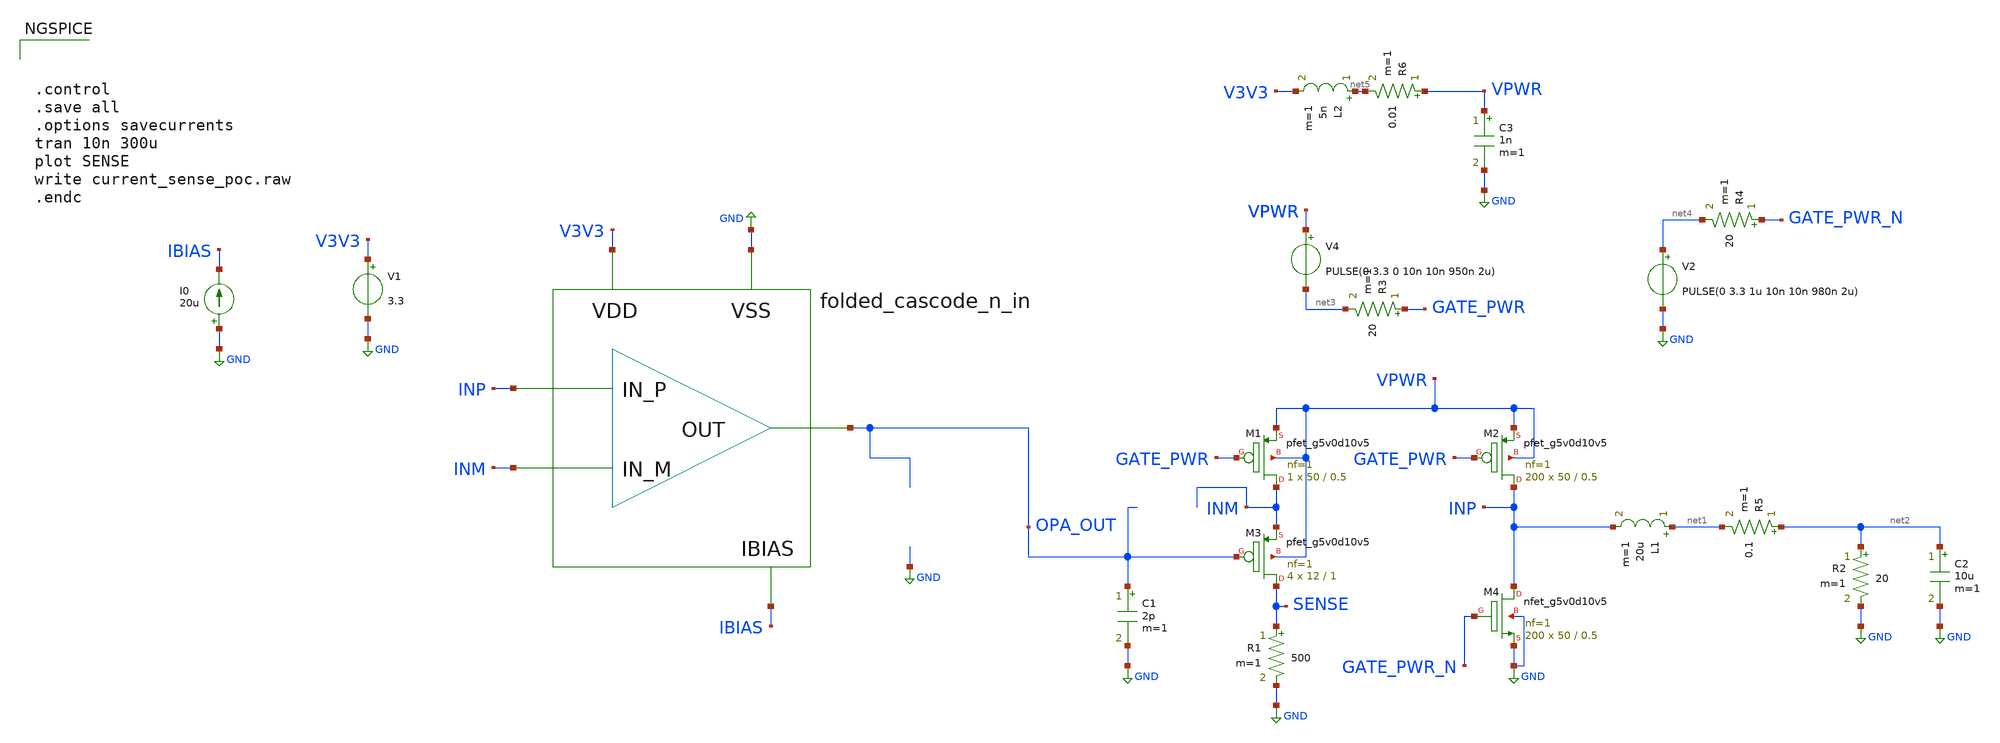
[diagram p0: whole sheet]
** sch_path: design/current-sense/current_sense_poc.sch
**.subckt current_sense_poc
V1 V3V3 GND 3.3
I0 GND IBIAS 20u
x1 INP INM OPA_OUT V3V3 GND IBIAS folded_cascode_n_in
XM1 INM GATE_PWR VPWR VPWR sky130_fd_pr__pfet_g5v0d10v5 L=0.5 W=50 nf=1 ad='int((nf+1)/2) * W/nf * 0.29'
+ as='int((nf+2)/2) * W/nf * 0.29' pd='2*int((nf+1)/2) * (W/nf + 0.29)' ps='2*int((nf+2)/2) * (W/nf + 0.29)'
+ nrd='0.29 / W' nrs='0.29 / W' sa=0 sb=0 sd=0 mult=1 m=1
XM2 INP GATE_PWR VPWR VPWR sky130_fd_pr__pfet_g5v0d10v5 L=0.5 W=50 nf=1 ad='int((nf+1)/2) * W/nf * 0.29'
+ as='int((nf+2)/2) * W/nf * 0.29' pd='2*int((nf+1)/2) * (W/nf + 0.29)' ps='2*int((nf+2)/2) * (W/nf + 0.29)'
+ nrd='0.29 / W' nrs='0.29 / W' sa=0 sb=0 sd=0 mult=200 m=200
V4 VPWR net3 PULSE(0 3.3 0 10n 10n 950n 2u)
XM3 SENSE OPA_OUT INM VPWR sky130_fd_pr__pfet_g5v0d10v5 L=1 W=12 nf=1 ad='int((nf+1)/2) * W/nf * 0.29'
+ as='int((nf+2)/2) * W/nf * 0.29' pd='2*int((nf+1)/2) * (W/nf + 0.29)' ps='2*int((nf+2)/2) * (W/nf + 0.29)'
+ nrd='0.29 / W' nrs='0.29 / W' sa=0 sb=0 sd=0 mult=4 m=4
R1 SENSE GND 500 m=1
R2 net2 GND 20 m=1
C1 OPA_OUT GND 2p m=1
L1 net1 INP 20u m=1
C2 net2 GND 10u m=1
R3 GATE_PWR net3 20 m=1
V2 net4 GND PULSE(0 3.3 1u 10n 10n 980n 2u)
R4 GATE_PWR_N net4 20 m=1
L2 net5 V3V3 5n m=1
C3 VPWR GND 1n m=1
XM4 INP GATE_PWR_N GND GND sky130_fd_pr__nfet_g5v0d10v5 L=0.5 W=50 nf=1 ad='int((nf+1)/2) * W/nf * 0.29'
+ as='int((nf+2)/2) * W/nf * 0.29' pd='2*int((nf+1)/2) * (W/nf + 0.29)' ps='2*int((nf+2)/2) * (W/nf + 0.29)'
+ nrd='0.29 / W' nrs='0.29 / W' sa=0 sb=0 sd=0 mult=200 m=200
R5 net2 net1 0.1 m=1
R6 VPWR net5 0.01 m=1
**** begin user architecture code



.control
.save all
.options savecurrents
tran 10n 300u
plot SENSE
write current_sense_poc.raw
.endc



.include $::SKYWATER_MODELS/cells/nfet_01v8/sky130_fd_pr__nfet_01v8__tt.corner.spice
.include $::SKYWATER_MODELS/cells/nfet_01v8_lvt/sky130_fd_pr__nfet_01v8_lvt__tt.corner.spice
.include $::SKYWATER_MODELS/cells/pfet_01v8/sky130_fd_pr__pfet_01v8__tt.corner.spice
.include $::SKYWATER_MODELS/cells/nfet_03v3_nvt/sky130_fd_pr__nfet_03v3_nvt__tt.corner.spice
.include $::SKYWATER_MODELS/cells/nfet_05v0_nvt/sky130_fd_pr__nfet_05v0_nvt__tt.corner.spice
.include $::SKYWATER_MODELS/cells/esd_nfet_01v8/sky130_fd_pr__esd_nfet_01v8__tt.corner.spice
.include $::SKYWATER_MODELS/cells/pfet_01v8_lvt/sky130_fd_pr__pfet_01v8_lvt__tt.corner.spice
.include $::SKYWATER_MODELS/cells/pfet_01v8_hvt/sky130_fd_pr__pfet_01v8_hvt__tt.corner.spice
.include $::SKYWATER_MODELS/cells/esd_pfet_g5v0d10v5/sky130_fd_pr__esd_pfet_g5v0d10v5__tt.corner.spice
.include $::SKYWATER_MODELS/cells/pfet_g5v0d10v5/sky130_fd_pr__pfet_g5v0d10v5__tt.corner.spice
.include $::SKYWATER_MODELS/cells/pfet_g5v0d16v0/sky130_fd_pr__pfet_g5v0d16v0__tt.corner.spice
.include $::SKYWATER_MODELS/cells/nfet_g5v0d10v5/sky130_fd_pr__nfet_g5v0d10v5__tt.corner.spice
.include $::SKYWATER_MODELS/cells/nfet_g5v0d16v0/sky130_fd_pr__nfet_g5v0d16v0__tt_discrete.corner.spice
.include $::SKYWATER_MODELS/cells/esd_nfet_g5v0d10v5/sky130_fd_pr__esd_nfet_g5v0d10v5__tt.corner.spice
.include $::SKYWATER_MODELS/models/corners/tt/nonfet.spice
* Mismatch parameters
.include $::SKYWATER_MODELS/cells/nfet_01v8/sky130_fd_pr__nfet_01v8__mismatch.corner.spice
.include $::SKYWATER_MODELS/cells/pfet_01v8/sky130_fd_pr__pfet_01v8__mismatch.corner.spice
.include $::SKYWATER_MODELS/cells/nfet_01v8_lvt/sky130_fd_pr__nfet_01v8_lvt__mismatch.corner.spice
.include $::SKYWATER_MODELS/cells/pfet_01v8_lvt/sky130_fd_pr__pfet_01v8_lvt__mismatch.corner.spice
.include $::SKYWATER_MODELS/cells/pfet_01v8_hvt/sky130_fd_pr__pfet_01v8_hvt__mismatch.corner.spice
.include $::SKYWATER_MODELS/cells/nfet_g5v0d10v5/sky130_fd_pr__nfet_g5v0d10v5__mismatch.corner.spice
.include $::SKYWATER_MODELS/cells/pfet_g5v0d10v5/sky130_fd_pr__pfet_g5v0d10v5__mismatch.corner.spice
.include $::SKYWATER_MODELS/cells/nfet_05v0_nvt/sky130_fd_pr__nfet_05v0_nvt__mismatch.corner.spice
.include $::SKYWATER_MODELS/cells/nfet_03v3_nvt/sky130_fd_pr__nfet_03v3_nvt__mismatch.corner.spice
* Resistor$::SKYWATER_MODELS/Capacitor
.include $::SKYWATER_MODELS/models/r+c/res_typical__cap_typical.spice
.include $::SKYWATER_MODELS/models/r+c/res_typical__cap_typical__lin.spice
* Special cells
.include $::SKYWATER_MODELS/models/corners/tt/specialized_cells.spice
* All models
.include $::SKYWATER_MODELS/models/all.spice
* Corner
.include $::SKYWATER_MODELS/models/corners/tt/rf.spice

**** end user architecture code
**.ends

* expanding   symbol:  design/folded-cascode-n-in/folded_cascode_n_in.sym # of pins=6
** sym_path: design/folded-cascode-n-in/folded_cascode_n_in.sym
** sch_path: design/folded-cascode-n-in/folded_cascode_n_in.sch
.subckt folded_cascode_n_in IN_P IN_M OUT VDD VSS VBN
*.ipin IN_P
*.ipin IN_M
*.ipin OUT
*.ipin VDD
*.ipin VSS
*.ipin VBN
XM1 net1 VBN VSS VSS sky130_fd_pr__nfet_g5v0d10v5 L=1 W=5 nf=1 ad='int((nf+1)/2) * W/nf * 0.29' as='int((nf+2)/2) * W/nf * 0.29'
+ pd='2*int((nf+1)/2) * (W/nf + 0.29)' ps='2*int((nf+2)/2) * (W/nf + 0.29)' nrd='0.29 / W' nrs='0.29 / W'
+ sa=0 sb=0 sd=0 mult=12 m=12
XM3 VS1_P IN_M net1 VSS sky130_fd_pr__nfet_g5v0d10v5 L=1 W=5 nf=1 ad='int((nf+1)/2) * W/nf * 0.29' as='int((nf+2)/2) * W/nf * 0.29'
+ pd='2*int((nf+1)/2) * (W/nf + 0.29)' ps='2*int((nf+2)/2) * (W/nf + 0.29)' nrd='0.29 / W' nrs='0.29 / W'
+ sa=0 sb=0 sd=0 mult=24 m=24
XM4 VS1_M IN_P net1 VSS sky130_fd_pr__nfet_g5v0d10v5 L=1 W=5 nf=1 ad='int((nf+1)/2) * W/nf * 0.29' as='int((nf+2)/2) * W/nf * 0.29'
+ pd='2*int((nf+1)/2) * (W/nf + 0.29)' ps='2*int((nf+2)/2) * (W/nf + 0.29)' nrd='0.29 / W' nrs='0.29 / W'
+ sa=0 sb=0 sd=0 mult=24 m=24
XM9 net2 VCN net4 VSS sky130_fd_pr__nfet_g5v0d10v5 L=1 W=5 nf=1 ad='int((nf+1)/2) * W/nf * 0.29' as='int((nf+2)/2) * W/nf * 0.29'
+ pd='2*int((nf+1)/2) * (W/nf + 0.29)' ps='2*int((nf+2)/2) * (W/nf + 0.29)' nrd='0.29 / W' nrs='0.29 / W'
+ sa=0 sb=0 sd=0 mult=3 m=3
XM10 net3 net2 VSS VSS sky130_fd_pr__nfet_g5v0d10v5 L=1 W=5 nf=1 ad='int((nf+1)/2) * W/nf * 0.29' as='int((nf+2)/2) * W/nf * 0.29'
+ pd='2*int((nf+1)/2) * (W/nf + 0.29)' ps='2*int((nf+2)/2) * (W/nf + 0.29)' nrd='0.29 / W' nrs='0.29 / W'
+ sa=0 sb=0 sd=0 mult=3 m=3
XM11 net4 net2 VSS VSS sky130_fd_pr__nfet_g5v0d10v5 L=1 W=5 nf=1 ad='int((nf+1)/2) * W/nf * 0.29' as='int((nf+2)/2) * W/nf * 0.29'
+ pd='2*int((nf+1)/2) * (W/nf + 0.29)' ps='2*int((nf+2)/2) * (W/nf + 0.29)' nrd='0.29 / W' nrs='0.29 / W'
+ sa=0 sb=0 sd=0 mult=3 m=3
XM12 OUT VCN net3 VSS sky130_fd_pr__nfet_g5v0d10v5 L=1 W=5 nf=1 ad='int((nf+1)/2) * W/nf * 0.29' as='int((nf+2)/2) * W/nf * 0.29'
+ pd='2*int((nf+1)/2) * (W/nf + 0.29)' ps='2*int((nf+2)/2) * (W/nf + 0.29)' nrd='0.29 / W' nrs='0.29 / W'
+ sa=0 sb=0 sd=0 mult=3 m=3
XM5 VS1_P VBP_INT VDD VDD sky130_fd_pr__pfet_g5v0d10v5 L=1 W=5 nf=1 ad='int((nf+1)/2) * W/nf * 0.29'
+ as='int((nf+2)/2) * W/nf * 0.29' pd='2*int((nf+1)/2) * (W/nf + 0.29)' ps='2*int((nf+2)/2) * (W/nf + 0.29)'
+ nrd='0.29 / W' nrs='0.29 / W' sa=0 sb=0 sd=0 mult=9 m=9
XM13 VS1_M VBP_INT VDD VDD sky130_fd_pr__pfet_g5v0d10v5 L=1 W=5 nf=1 ad='int((nf+1)/2) * W/nf * 0.29'
+ as='int((nf+2)/2) * W/nf * 0.29' pd='2*int((nf+1)/2) * (W/nf + 0.29)' ps='2*int((nf+2)/2) * (W/nf + 0.29)'
+ nrd='0.29 / W' nrs='0.29 / W' sa=0 sb=0 sd=0 mult=9 m=9
XM17 VBP_INT VBN VSS VSS sky130_fd_pr__nfet_g5v0d10v5 L=1 W=5 nf=1 ad='int((nf+1)/2) * W/nf * 0.29' as='int((nf+2)/2) * W/nf * 0.29'
+ pd='2*int((nf+1)/2) * (W/nf + 0.29)' ps='2*int((nf+2)/2) * (W/nf + 0.29)' nrd='0.29 / W' nrs='0.29 / W'
+ sa=0 sb=0 sd=0 mult=1 m=1
XM18 VBP_INT VBP_INT VDD VDD sky130_fd_pr__pfet_g5v0d10v5 L=1 W=5 nf=1 ad='int((nf+1)/2) * W/nf * 0.29'
+ as='int((nf+2)/2) * W/nf * 0.29' pd='2*int((nf+1)/2) * (W/nf + 0.29)' ps='2*int((nf+2)/2) * (W/nf + 0.29)'
+ nrd='0.29 / W' nrs='0.29 / W' sa=0 sb=0 sd=0 mult=1 m=1
XM14 net2 VCP VS1_M VDD sky130_fd_pr__pfet_g5v0d10v5 L=1 W=5 nf=1 ad='int((nf+1)/2) * W/nf * 0.29' as='int((nf+2)/2) * W/nf * 0.29'
+ pd='2*int((nf+1)/2) * (W/nf + 0.29)' ps='2*int((nf+2)/2) * (W/nf + 0.29)' nrd='0.29 / W' nrs='0.29 / W'
+ sa=0 sb=0 sd=0 mult=3 m=3
XM19 OUT VCP VS1_P VDD sky130_fd_pr__pfet_g5v0d10v5 L=1 W=5 nf=1 ad='int((nf+1)/2) * W/nf * 0.29' as='int((nf+2)/2) * W/nf * 0.29'
+ pd='2*int((nf+1)/2) * (W/nf + 0.29)' ps='2*int((nf+2)/2) * (W/nf + 0.29)' nrd='0.29 / W' nrs='0.29 / W'
+ sa=0 sb=0 sd=0 mult=3 m=3
XM2 VBP_INT VBP_INT VS1_P VSS sky130_fd_pr__nfet_g5v0d10v5 L=1 W=5 nf=1 ad='int((nf+1)/2) * W/nf * 0.29'
+ as='int((nf+2)/2) * W/nf * 0.29' pd='2*int((nf+1)/2) * (W/nf + 0.29)' ps='2*int((nf+2)/2) * (W/nf + 0.29)'
+ nrd='0.29 / W' nrs='0.29 / W' sa=0 sb=0 sd=0 mult=1 m=1
XM6 VBP_INT VBP_INT VS1_M VSS sky130_fd_pr__nfet_g5v0d10v5 L=1 W=5 nf=1 ad='int((nf+1)/2) * W/nf * 0.29'
+ as='int((nf+2)/2) * W/nf * 0.29' pd='2*int((nf+1)/2) * (W/nf + 0.29)' ps='2*int((nf+2)/2) * (W/nf + 0.29)'
+ nrd='0.29 / W' nrs='0.29 / W' sa=0 sb=0 sd=0 mult=1 m=1
XM7 VBP VBP VDD VDD sky130_fd_pr__pfet_g5v0d10v5 L=1 W=5 nf=1 ad='int((nf+1)/2) * W/nf * 0.29' as='int((nf+2)/2) * W/nf * 0.29'
+ pd='2*int((nf+1)/2) * (W/nf + 0.29)' ps='2*int((nf+2)/2) * (W/nf + 0.29)' nrd='0.29 / W' nrs='0.29 / W'
+ sa=0 sb=0 sd=0 mult=1 m=1
XM8 net5 VBP net12 VDD sky130_fd_pr__pfet_g5v0d10v5 L=1 W=5 nf=1 ad='int((nf+1)/2) * W/nf * 0.29' as='int((nf+2)/2) * W/nf * 0.29'
+ pd='2*int((nf+1)/2) * (W/nf + 0.29)' ps='2*int((nf+2)/2) * (W/nf + 0.29)' nrd='0.29 / W' nrs='0.29 / W'
+ sa=0 sb=0 sd=0 mult=1 m=1
XM15 VCN VBP VDD VDD sky130_fd_pr__pfet_g5v0d10v5 L=1 W=5 nf=1 ad='int((nf+1)/2) * W/nf * 0.29' as='int((nf+2)/2) * W/nf * 0.29'
+ pd='2*int((nf+1)/2) * (W/nf + 0.29)' ps='2*int((nf+2)/2) * (W/nf + 0.29)' nrd='0.29 / W' nrs='0.29 / W'
+ sa=0 sb=0 sd=0 mult=1 m=1
XM16 net5 net5 net6 VSS sky130_fd_pr__nfet_g5v0d10v5 L=1 W=5 nf=1 ad='int((nf+1)/2) * W/nf * 0.29' as='int((nf+2)/2) * W/nf * 0.29'
+ pd='2*int((nf+1)/2) * (W/nf + 0.29)' ps='2*int((nf+2)/2) * (W/nf + 0.29)' nrd='0.29 / W' nrs='0.29 / W'
+ sa=0 sb=0 sd=0 mult=2 m=2
XM20 net6 net5 VSS VSS sky130_fd_pr__nfet_g5v0d10v5 L=1 W=5 nf=1 ad='int((nf+1)/2) * W/nf * 0.29' as='int((nf+2)/2) * W/nf * 0.29'
+ pd='2*int((nf+1)/2) * (W/nf + 0.29)' ps='2*int((nf+2)/2) * (W/nf + 0.29)' nrd='0.29 / W' nrs='0.29 / W'
+ sa=0 sb=0 sd=0 mult=1 m=1
XM21 VCN VCN net6 VSS sky130_fd_pr__nfet_g5v0d10v5 L=1 W=5 nf=1 ad='int((nf+1)/2) * W/nf * 0.29' as='int((nf+2)/2) * W/nf * 0.29'
+ pd='2*int((nf+1)/2) * (W/nf + 0.29)' ps='2*int((nf+2)/2) * (W/nf + 0.29)' nrd='0.29 / W' nrs='0.29 / W'
+ sa=0 sb=0 sd=0 mult=1 m=1
XM24 net7 VBN net10 VSS sky130_fd_pr__nfet_g5v0d10v5 L=1 W=5 nf=1 ad='int((nf+1)/2) * W/nf * 0.29' as='int((nf+2)/2) * W/nf * 0.29'
+ pd='2*int((nf+1)/2) * (W/nf + 0.29)' ps='2*int((nf+2)/2) * (W/nf + 0.29)' nrd='0.29 / W' nrs='0.29 / W'
+ sa=0 sb=0 sd=0 mult=1 m=1
XM25 VCP VBN VSS VSS sky130_fd_pr__nfet_g5v0d10v5 L=1 W=5 nf=1 ad='int((nf+1)/2) * W/nf * 0.29' as='int((nf+2)/2) * W/nf * 0.29'
+ pd='2*int((nf+1)/2) * (W/nf + 0.29)' ps='2*int((nf+2)/2) * (W/nf + 0.29)' nrd='0.29 / W' nrs='0.29 / W'
+ sa=0 sb=0 sd=0 mult=1 m=1
XM26 net7 net7 net8 VDD sky130_fd_pr__pfet_g5v0d10v5 L=1 W=5 nf=1 ad='int((nf+1)/2) * W/nf * 0.29' as='int((nf+2)/2) * W/nf * 0.29'
+ pd='2*int((nf+1)/2) * (W/nf + 0.29)' ps='2*int((nf+2)/2) * (W/nf + 0.29)' nrd='0.29 / W' nrs='0.29 / W'
+ sa=0 sb=0 sd=0 mult=2 m=2
XM27 VCP VCP net8 VDD sky130_fd_pr__pfet_g5v0d10v5 L=1 W=5 nf=1 ad='int((nf+1)/2) * W/nf * 0.29' as='int((nf+2)/2) * W/nf * 0.29'
+ pd='2*int((nf+1)/2) * (W/nf + 0.29)' ps='2*int((nf+2)/2) * (W/nf + 0.29)' nrd='0.29 / W' nrs='0.29 / W'
+ sa=0 sb=0 sd=0 mult=1 m=1
XM28 net8 net7 VDD VDD sky130_fd_pr__pfet_g5v0d10v5 L=1 W=5 nf=1 ad='int((nf+1)/2) * W/nf * 0.29' as='int((nf+2)/2) * W/nf * 0.29'
+ pd='2*int((nf+1)/2) * (W/nf + 0.29)' ps='2*int((nf+2)/2) * (W/nf + 0.29)' nrd='0.29 / W' nrs='0.29 / W'
+ sa=0 sb=0 sd=0 mult=1 m=1
XM29 VBP VBN VSS VSS sky130_fd_pr__nfet_g5v0d10v5 L=1 W=5 nf=1 ad='int((nf+1)/2) * W/nf * 0.29' as='int((nf+2)/2) * W/nf * 0.29'
+ pd='2*int((nf+1)/2) * (W/nf + 0.29)' ps='2*int((nf+2)/2) * (W/nf + 0.29)' nrd='0.29 / W' nrs='0.29 / W'
+ sa=0 sb=0 sd=0 mult=1 m=1
XM32 net12 VBP net9 VDD sky130_fd_pr__pfet_g5v0d10v5 L=1 W=5 nf=1 ad='int((nf+1)/2) * W/nf * 0.29' as='int((nf+2)/2) * W/nf * 0.29'
+ pd='2*int((nf+1)/2) * (W/nf + 0.29)' ps='2*int((nf+2)/2) * (W/nf + 0.29)' nrd='0.29 / W' nrs='0.29 / W'
+ sa=0 sb=0 sd=0 mult=1 m=1
XM33 net9 VBP VDD VDD sky130_fd_pr__pfet_g5v0d10v5 L=1 W=5 nf=1 ad='int((nf+1)/2) * W/nf * 0.29' as='int((nf+2)/2) * W/nf * 0.29'
+ pd='2*int((nf+1)/2) * (W/nf + 0.29)' ps='2*int((nf+2)/2) * (W/nf + 0.29)' nrd='0.29 / W' nrs='0.29 / W'
+ sa=0 sb=0 sd=0 mult=1 m=1
XM34 net10 VBN net11 VSS sky130_fd_pr__nfet_g5v0d10v5 L=1 W=5 nf=1 ad='int((nf+1)/2) * W/nf * 0.29' as='int((nf+2)/2) * W/nf * 0.29'
+ pd='2*int((nf+1)/2) * (W/nf + 0.29)' ps='2*int((nf+2)/2) * (W/nf + 0.29)' nrd='0.29 / W' nrs='0.29 / W'
+ sa=0 sb=0 sd=0 mult=1 m=1
XM35 net11 VBN VSS VSS sky130_fd_pr__nfet_g5v0d10v5 L=1 W=5 nf=1 ad='int((nf+1)/2) * W/nf * 0.29' as='int((nf+2)/2) * W/nf * 0.29'
+ pd='2*int((nf+1)/2) * (W/nf + 0.29)' ps='2*int((nf+2)/2) * (W/nf + 0.29)' nrd='0.29 / W' nrs='0.29 / W'
+ sa=0 sb=0 sd=0 mult=1 m=1
XM30 VBN VBN VSS VSS sky130_fd_pr__nfet_g5v0d10v5 L=1 W=5 nf=1 ad='int((nf+1)/2) * W/nf * 0.29' as='int((nf+2)/2) * W/nf * 0.29'
+ pd='2*int((nf+1)/2) * (W/nf + 0.29)' ps='2*int((nf+2)/2) * (W/nf + 0.29)' nrd='0.29 / W' nrs='0.29 / W'
+ sa=0 sb=0 sd=0 mult=1 m=1
.ends

.GLOBAL GND
**** begin user architecture code
[sky130_models]
**** end user architecture code
.end
